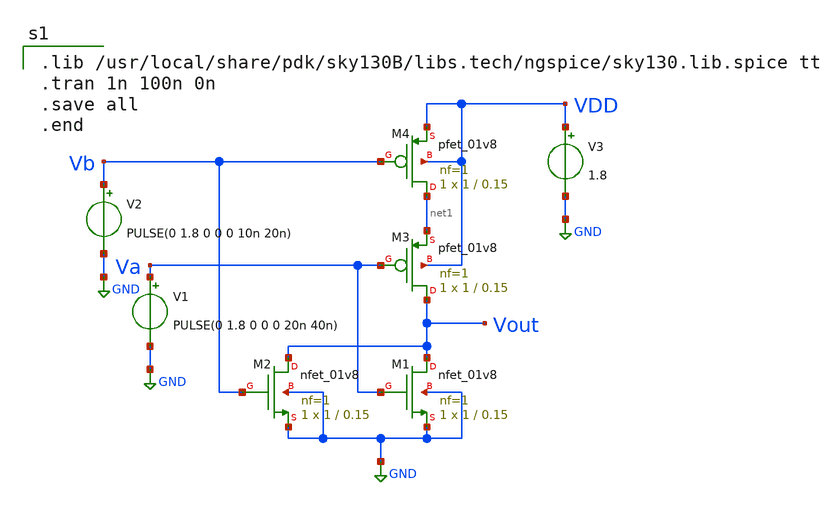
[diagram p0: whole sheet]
** sch_path: physical_design_layout_of_2_input_nor_gate/nor2gate_layout.sch
**.subckt nor2gate_layout
XM1 Vout Va GND GND sky130_fd_pr__nfet_01v8 L=0.15 W=1 nf=1 ad='int((nf+1)/2) * W/nf * 0.29' as='int((nf+2)/2) * W/nf * 0.29'
+ pd='2*int((nf+1)/2) * (W/nf + 0.29)' ps='2*int((nf+2)/2) * (W/nf + 0.29)' nrd='0.29 / W' nrs='0.29 / W'
+ sa=0 sb=0 sd=0 mult=1 m=1
XM2 Vout Vb GND GND sky130_fd_pr__nfet_01v8 L=0.15 W=1 nf=1 ad='int((nf+1)/2) * W/nf * 0.29' as='int((nf+2)/2) * W/nf * 0.29'
+ pd='2*int((nf+1)/2) * (W/nf + 0.29)' ps='2*int((nf+2)/2) * (W/nf + 0.29)' nrd='0.29 / W' nrs='0.29 / W'
+ sa=0 sb=0 sd=0 mult=1 m=1
XM3 Vout Va net1 VDD sky130_fd_pr__pfet_01v8 L=0.15 W=1 nf=1 ad='int((nf+1)/2) * W/nf * 0.29' as='int((nf+2)/2) * W/nf * 0.29'
+ pd='2*int((nf+1)/2) * (W/nf + 0.29)' ps='2*int((nf+2)/2) * (W/nf + 0.29)' nrd='0.29 / W' nrs='0.29 / W'
+ sa=0 sb=0 sd=0 mult=1 m=1
XM4 net1 Vb VDD VDD sky130_fd_pr__pfet_01v8 L=0.15 W=1 nf=1 ad='int((nf+1)/2) * W/nf * 0.29' as='int((nf+2)/2) * W/nf * 0.29'
+ pd='2*int((nf+1)/2) * (W/nf + 0.29)' ps='2*int((nf+2)/2) * (W/nf + 0.29)' nrd='0.29 / W' nrs='0.29 / W'
+ sa=0 sb=0 sd=0 mult=1 m=1
V1 Va GND PULSE(0 1.8 0 0 0 20n 40n)
V2 Vb GND PULSE(0 1.8 0 0 0 10n 20n)
V3 VDD GND 1.8
**** begin user architecture code

.lib /usr/local/share/pdk/sky130B/libs.tech/ngspice/sky130.lib.spice tt
.tran 1n 100n 0n
.save all
.end


**** end user architecture code
**.ends
.GLOBAL GND
.end
